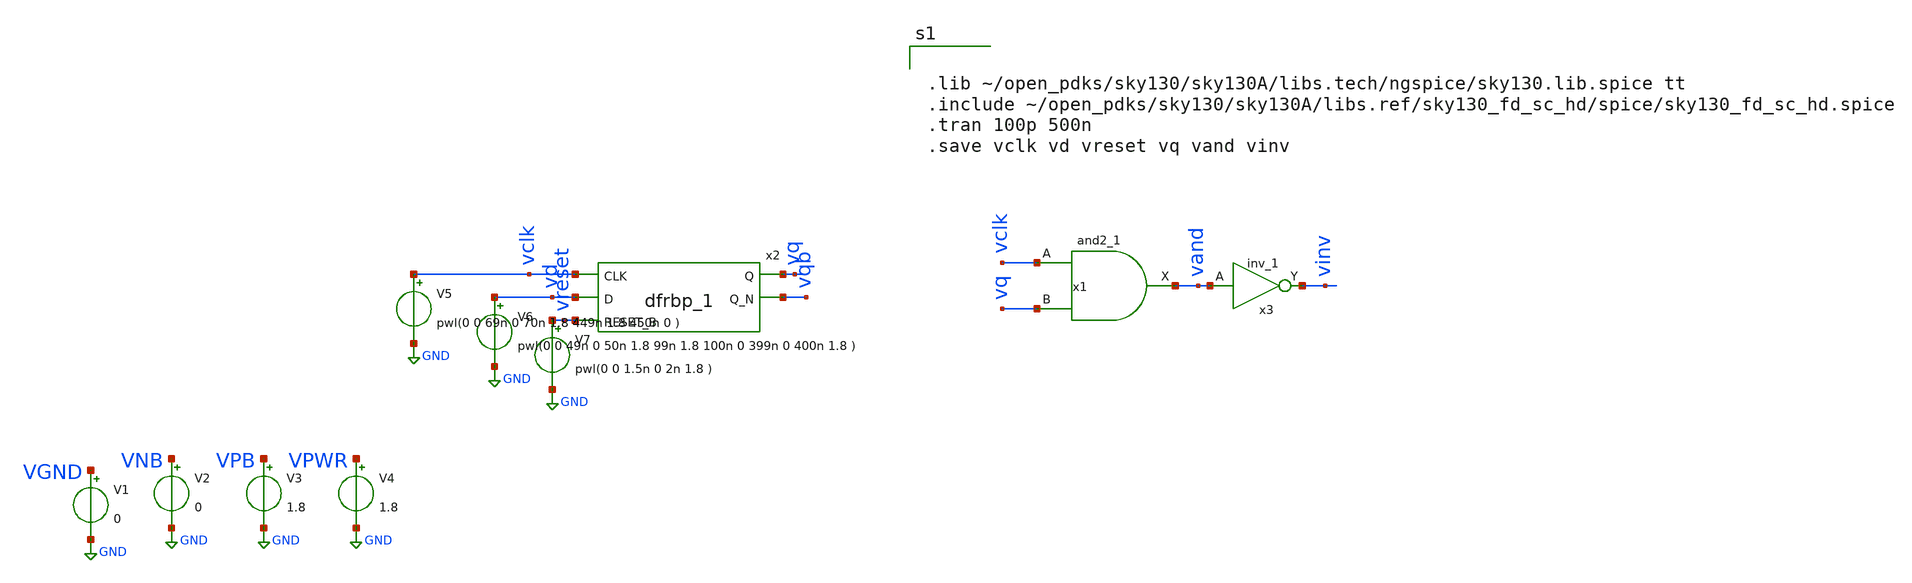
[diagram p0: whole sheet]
** sch_path: one_switch.sch
**.subckt one_switch
x2 vclk vd vreset VGND VNB VPB VPWR vq vqb sky130_fd_sc_hd__dfrbp_1
V1 VGND GND 0
V2 VNB GND 0
V3 VPB GND 1.8
V4 VPWR GND 1.8
V5 vclk GND pwl(0 0 69n 0 70n 1.8 449n 1.8 450n 0 )
V6 vd GND pwl(0 0 49n 0 50n 1.8 99n 1.8 100n 0 399n 0 400n 1.8 )
V7 vreset GND pwl(0 0 1.5n 0 2n 1.8 )
x1 vclk vq VGND VNB VPB VPWR vand sky130_fd_sc_hd__and2_1
x3 vand VGND VNB VPB VPWR vinv sky130_fd_sc_hd__inv_1
**** begin user architecture code


.lib ~/open_pdks/sky130/sky130A/libs.tech/ngspice/sky130.lib.spice tt
.include ~/open_pdks/sky130/sky130A/libs.ref/sky130_fd_sc_hd/spice/sky130_fd_sc_hd.spice
.tran 100p 500n
.save vclk vd vreset vq vand vinv

**** end user architecture code
**.ends
.GLOBAL GND
.end
